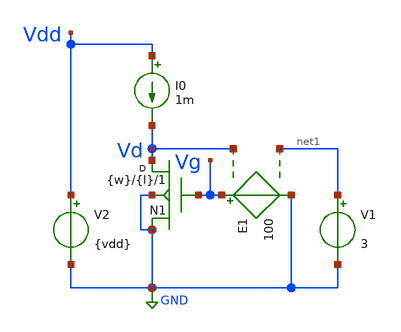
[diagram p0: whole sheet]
** sch_path: Parametros_Vaf/sigma_test.sch
**.subckt sigma_test
N1 Vd Vg GND GND NMOS_ACM w={w} l={l} m=1
E1 Vg GND Vd net1 100
I0 Vdd Vd 1m
V1 net1 GND 3
V2 Vdd GND {vdd}
**** begin user architecture code


* Circuit Parameters
.param vd = 3
.param vdd = 1.2
.param step = 0.01
.param w = 5.0u
.param l = 0.18u
* Include Models
.model NMOS_ACM nmos_ACM
.model PMOS_ACM pmos_ACM
* OP Parameters & Singals to save
.save all
*Simulations
.dc V1 0 {vg} {step}
.control
pre_osdi NMOS_ACM_2V0.osdi
pre_osdi PMOS_ACM_2V0.osdi
run
let gm_id = deriv(-1*i(V2))/(-1*i(V2))
setplot dc1
plot gm_id
set filetype = ascii
write dcsweep.raw
.endc
.end


**** end user architecture code
**.ends
.GLOBAL GND
.end
